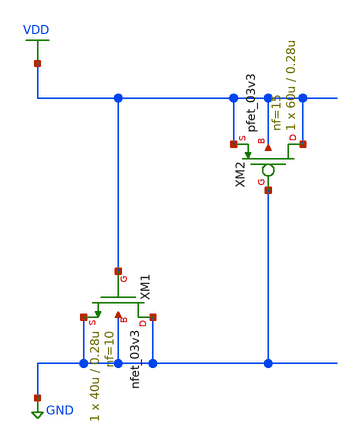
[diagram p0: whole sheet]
** sch_path: Schematic/break_before_make/decap_12.sch
**.subckt decap_12
XM1 GND VDD GND GND nfet_03v3 L=0.28u W=40u nf=10 ad='int((nf+1)/2) * W/nf * 0.18u' as='int((nf+2)/2) * W/nf * 0.18u'
+ pd='2*int((nf+1)/2) * (W/nf + 0.18u)' ps='2*int((nf+2)/2) * (W/nf + 0.18u)' nrd='0.18u / W' nrs='0.18u / W'
+ sa=0 sb=0 sd=0 m=1
XM2 VDD GND VDD VDD pfet_03v3 L=0.28u W=60u nf=15 ad='int((nf+1)/2) * W/nf * 0.18u' as='int((nf+2)/2) * W/nf * 0.18u'
+ pd='2*int((nf+1)/2) * (W/nf + 0.18u)' ps='2*int((nf+2)/2) * (W/nf + 0.18u)' nrd='0.18u / W' nrs='0.18u / W'
+ sa=0 sb=0 sd=0 m=1
**.ends
.GLOBAL VDD
.GLOBAL GND
.end
